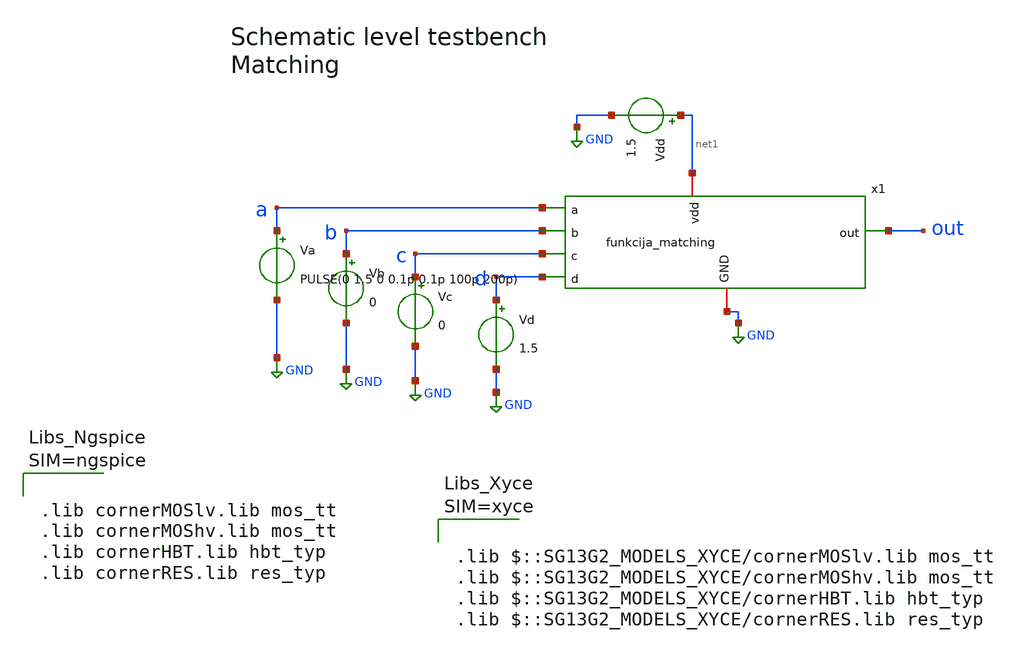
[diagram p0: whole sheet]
** sch_path: projekat/slucaj_2/testbench/tb_tran_matching.sch
**.subckt tb_tran_matching
Va a GND PULSE(0 1.5 0 0.1p 0.1p 100p 200p)
Vb b GND 0
Vc c GND 0
Vd d GND 1.5
Vdd net1 GND 1.5
x1 net1 out d a c b GND funkcija_matching
**** begin user architecture code



.lib cornerMOSlv.lib mos_tt
.lib cornerMOShv.lib mos_tt
.lib cornerHBT.lib hbt_typ
.lib cornerRES.lib res_typ









.tran 0.1p 500p

.control
  save all
  run

  meas tran tr_out TRIG v(out) VAL=0.15 RISE=2 TARG v(out) VAL=1.35 RISE=2
  meas tran tf_out TRIG v(out) VAL=1.35 FALL=2 TARG v(out) VAL=0.15 FALL=2

  plot v(a)+4.5 v(b)+3 v(c)+1.5 v(out)
  wrdata /home/Nikola.Jankovic/projekat/slucaj_2/python/odziv_2_matching.txt v(a) v(out)
  print tr_out tf_out
.endc

**** end user architecture code
**.ends
.GLOBAL GND
.end
